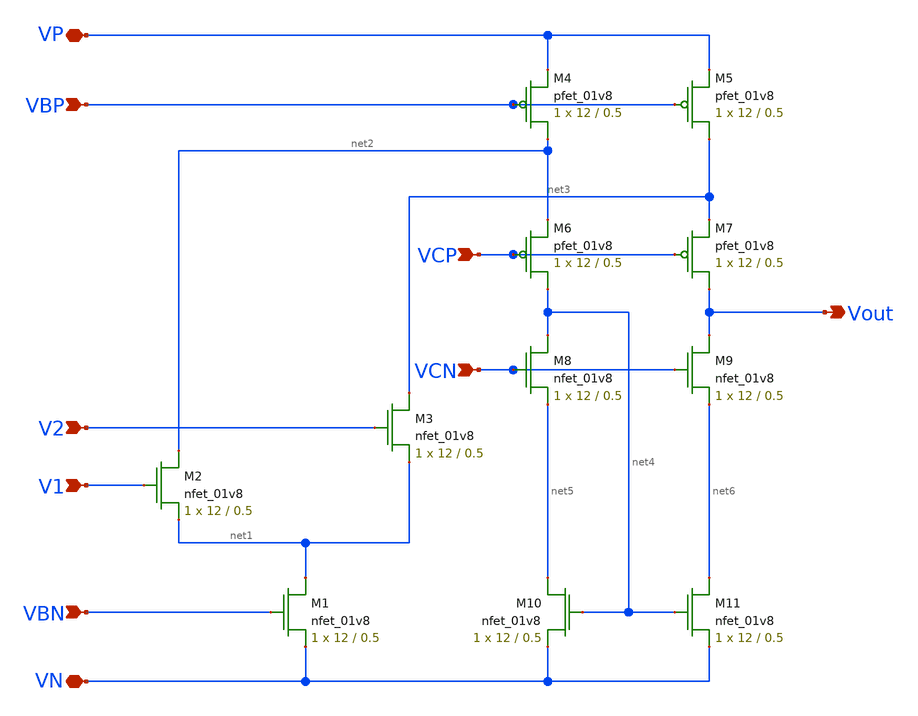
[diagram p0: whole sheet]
** sch_path: mp3/diff_amp/diff_amp.sch
**.subckt diff_amp V1 V2 VN VBN VBP VP VCP VCN Vout
*.ipin V1
*.ipin V2
*.iopin VN
*.ipin VBN
*.ipin VBP
*.iopin VP
*.ipin VCP
*.ipin VCN
*.opin Vout
XM1 net1 VBN VN VN sky130_fd_pr__nfet_01v8 L=0.5 W=12 nf=1 ad='int((nf+1)/2) * W/nf * 0.29' as='int((nf+2)/2) * W/nf * 0.29'
+ pd='2*int((nf+1)/2) * (W/nf + 0.29)' ps='2*int((nf+2)/2) * (W/nf + 0.29)' nrd='0.29 / W' nrs='0.29 / W'
+ sa=0 sb=0 sd=0 mult=1 m=1
XM2 net2 V1 net1 VN sky130_fd_pr__nfet_01v8 L=0.5 W=12 nf=1 ad='int((nf+1)/2) * W/nf * 0.29' as='int((nf+2)/2) * W/nf * 0.29'
+ pd='2*int((nf+1)/2) * (W/nf + 0.29)' ps='2*int((nf+2)/2) * (W/nf + 0.29)' nrd='0.29 / W' nrs='0.29 / W'
+ sa=0 sb=0 sd=0 mult=1 m=1
XM3 net3 V2 net1 VN sky130_fd_pr__nfet_01v8 L=0.5 W=12 nf=1 ad='int((nf+1)/2) * W/nf * 0.29' as='int((nf+2)/2) * W/nf * 0.29'
+ pd='2*int((nf+1)/2) * (W/nf + 0.29)' ps='2*int((nf+2)/2) * (W/nf + 0.29)' nrd='0.29 / W' nrs='0.29 / W'
+ sa=0 sb=0 sd=0 mult=1 m=1
XM4 net2 VBP VP VP sky130_fd_pr__pfet_01v8 L=0.5 W=12 nf=1 ad='int((nf+1)/2) * W/nf * 0.29' as='int((nf+2)/2) * W/nf * 0.29'
+ pd='2*int((nf+1)/2) * (W/nf + 0.29)' ps='2*int((nf+2)/2) * (W/nf + 0.29)' nrd='0.29 / W' nrs='0.29 / W'
+ sa=0 sb=0 sd=0 mult=1 m=1
XM5 net3 VBP VP VP sky130_fd_pr__pfet_01v8 L=0.5 W=12 nf=1 ad='int((nf+1)/2) * W/nf * 0.29' as='int((nf+2)/2) * W/nf * 0.29'
+ pd='2*int((nf+1)/2) * (W/nf + 0.29)' ps='2*int((nf+2)/2) * (W/nf + 0.29)' nrd='0.29 / W' nrs='0.29 / W'
+ sa=0 sb=0 sd=0 mult=1 m=1
XM6 net4 VCP net2 VP sky130_fd_pr__pfet_01v8 L=0.5 W=12 nf=1 ad='int((nf+1)/2) * W/nf * 0.29' as='int((nf+2)/2) * W/nf * 0.29'
+ pd='2*int((nf+1)/2) * (W/nf + 0.29)' ps='2*int((nf+2)/2) * (W/nf + 0.29)' nrd='0.29 / W' nrs='0.29 / W'
+ sa=0 sb=0 sd=0 mult=1 m=1
XM7 Vout VCP net3 VP sky130_fd_pr__pfet_01v8 L=0.5 W=12 nf=1 ad='int((nf+1)/2) * W/nf * 0.29' as='int((nf+2)/2) * W/nf * 0.29'
+ pd='2*int((nf+1)/2) * (W/nf + 0.29)' ps='2*int((nf+2)/2) * (W/nf + 0.29)' nrd='0.29 / W' nrs='0.29 / W'
+ sa=0 sb=0 sd=0 mult=1 m=1
XM8 net4 VCN net5 VN sky130_fd_pr__nfet_01v8 L=0.5 W=12 nf=1 ad='int((nf+1)/2) * W/nf * 0.29' as='int((nf+2)/2) * W/nf * 0.29'
+ pd='2*int((nf+1)/2) * (W/nf + 0.29)' ps='2*int((nf+2)/2) * (W/nf + 0.29)' nrd='0.29 / W' nrs='0.29 / W'
+ sa=0 sb=0 sd=0 mult=1 m=1
XM9 Vout VCN net6 VN sky130_fd_pr__nfet_01v8 L=0.5 W=12 nf=1 ad='int((nf+1)/2) * W/nf * 0.29' as='int((nf+2)/2) * W/nf * 0.29'
+ pd='2*int((nf+1)/2) * (W/nf + 0.29)' ps='2*int((nf+2)/2) * (W/nf + 0.29)' nrd='0.29 / W' nrs='0.29 / W'
+ sa=0 sb=0 sd=0 mult=1 m=1
XM10 net5 net4 VN VN sky130_fd_pr__nfet_01v8 L=0.5 W=12 nf=1 ad='int((nf+1)/2) * W/nf * 0.29' as='int((nf+2)/2) * W/nf * 0.29'
+ pd='2*int((nf+1)/2) * (W/nf + 0.29)' ps='2*int((nf+2)/2) * (W/nf + 0.29)' nrd='0.29 / W' nrs='0.29 / W'
+ sa=0 sb=0 sd=0 mult=1 m=1
XM11 net6 net4 VN VN sky130_fd_pr__nfet_01v8 L=0.5 W=12 nf=1 ad='int((nf+1)/2) * W/nf * 0.29' as='int((nf+2)/2) * W/nf * 0.29'
+ pd='2*int((nf+1)/2) * (W/nf + 0.29)' ps='2*int((nf+2)/2) * (W/nf + 0.29)' nrd='0.29 / W' nrs='0.29 / W'
+ sa=0 sb=0 sd=0 mult=1 m=1
**.ends
.end
